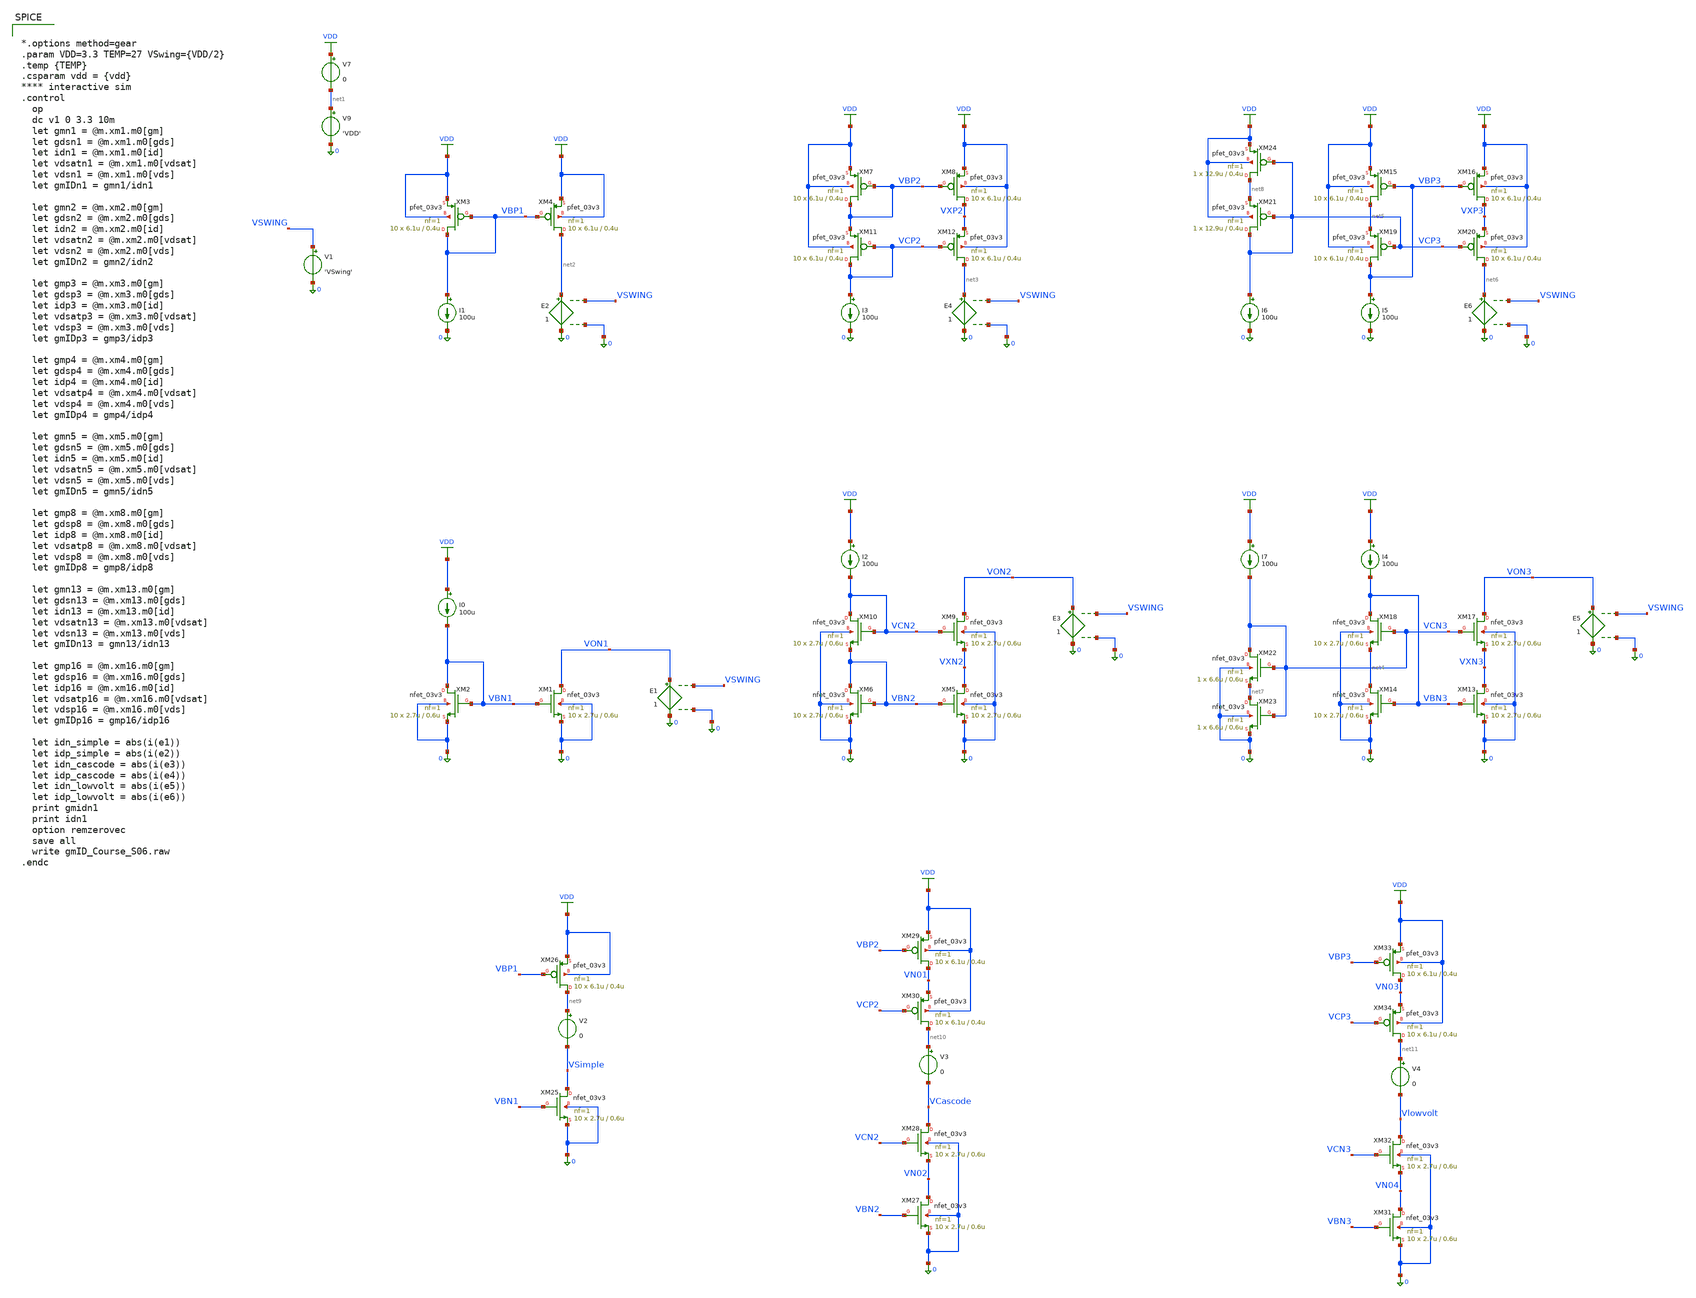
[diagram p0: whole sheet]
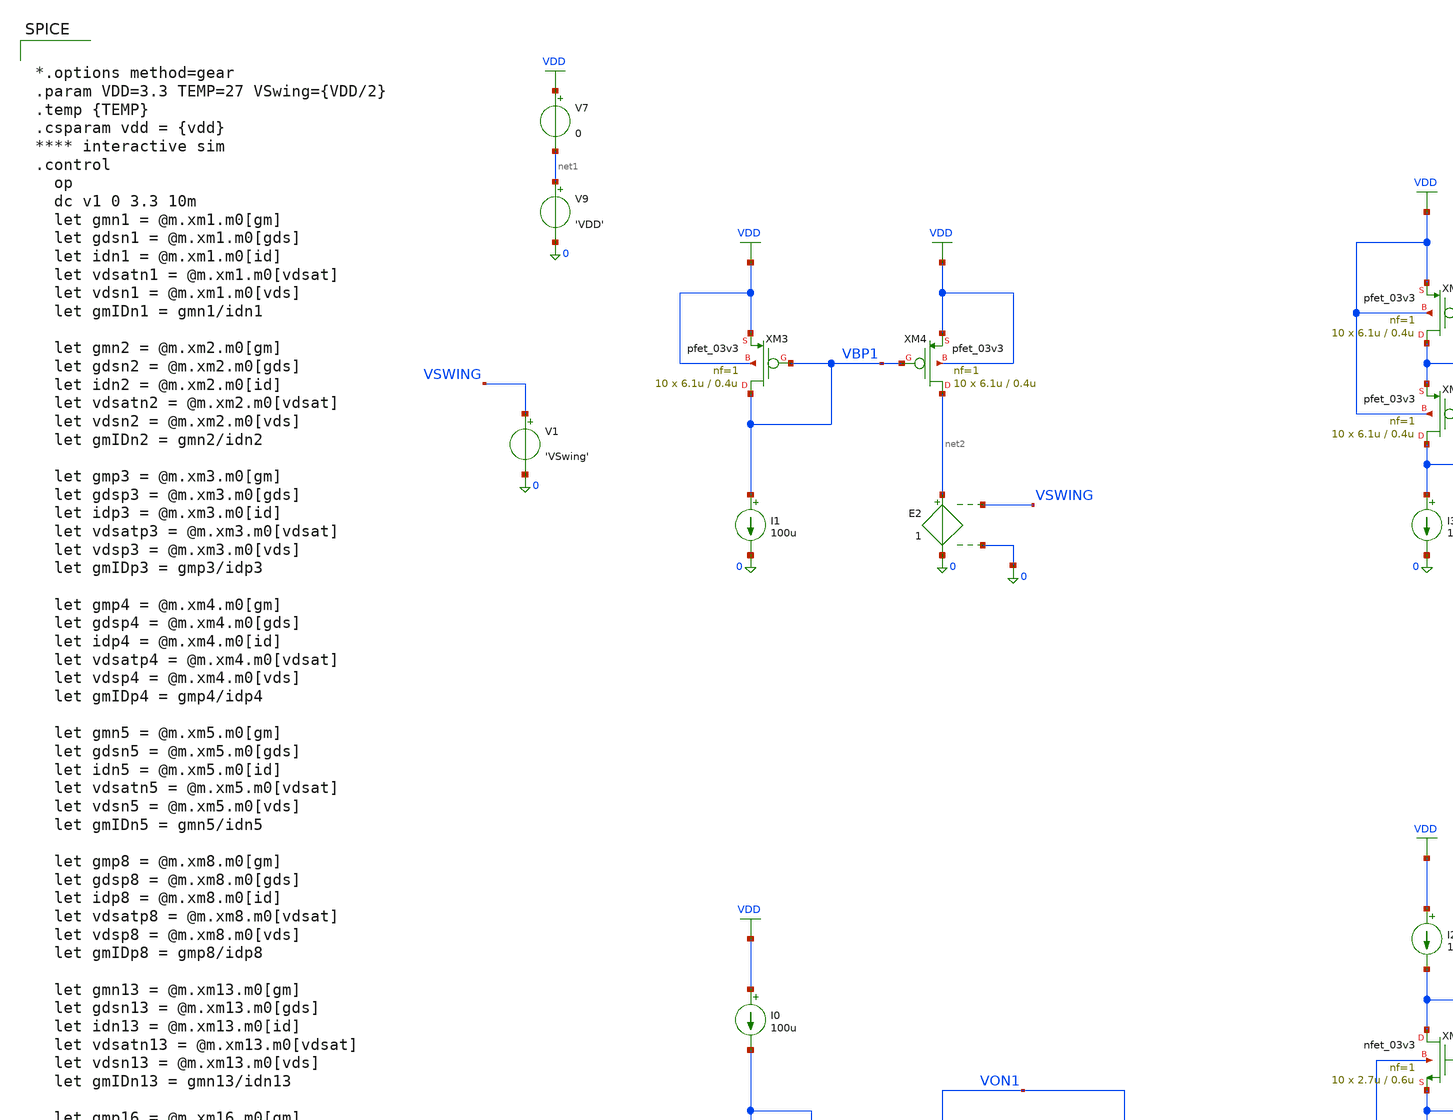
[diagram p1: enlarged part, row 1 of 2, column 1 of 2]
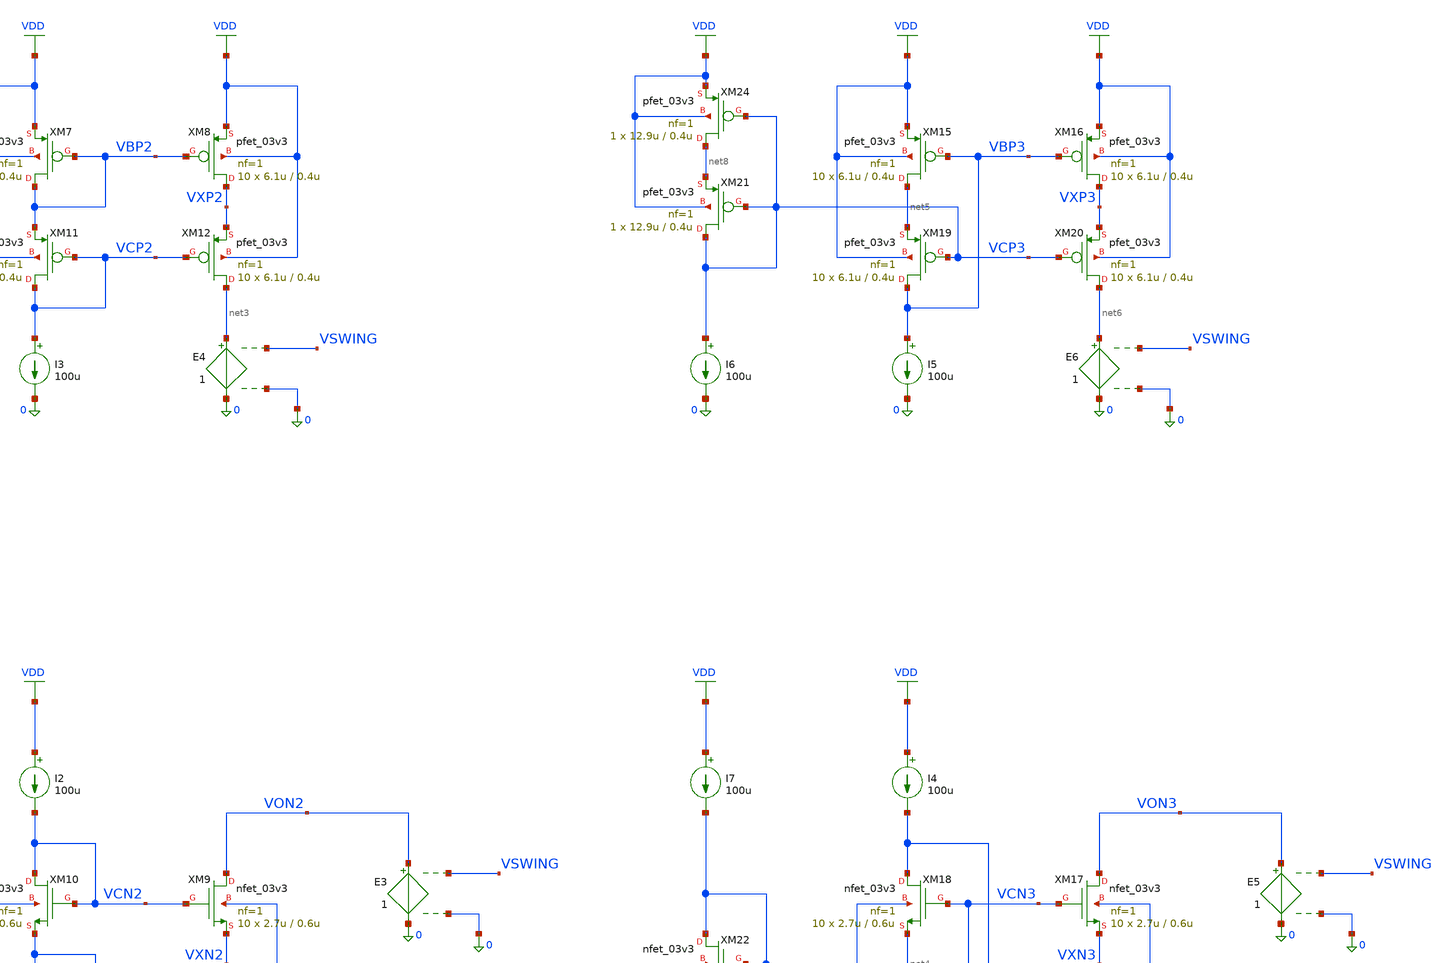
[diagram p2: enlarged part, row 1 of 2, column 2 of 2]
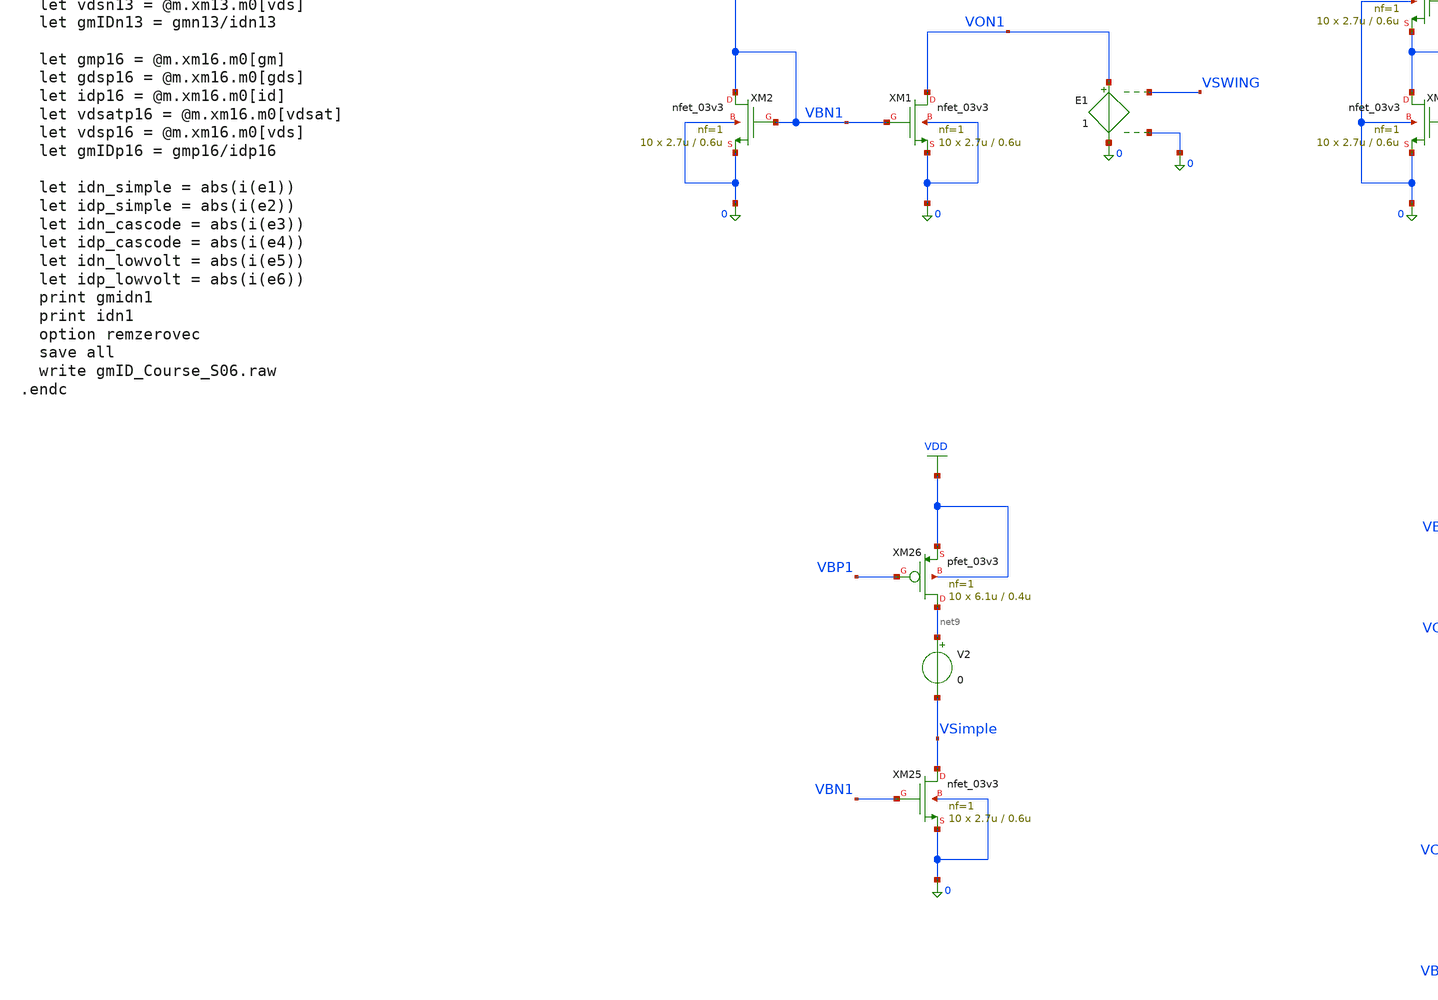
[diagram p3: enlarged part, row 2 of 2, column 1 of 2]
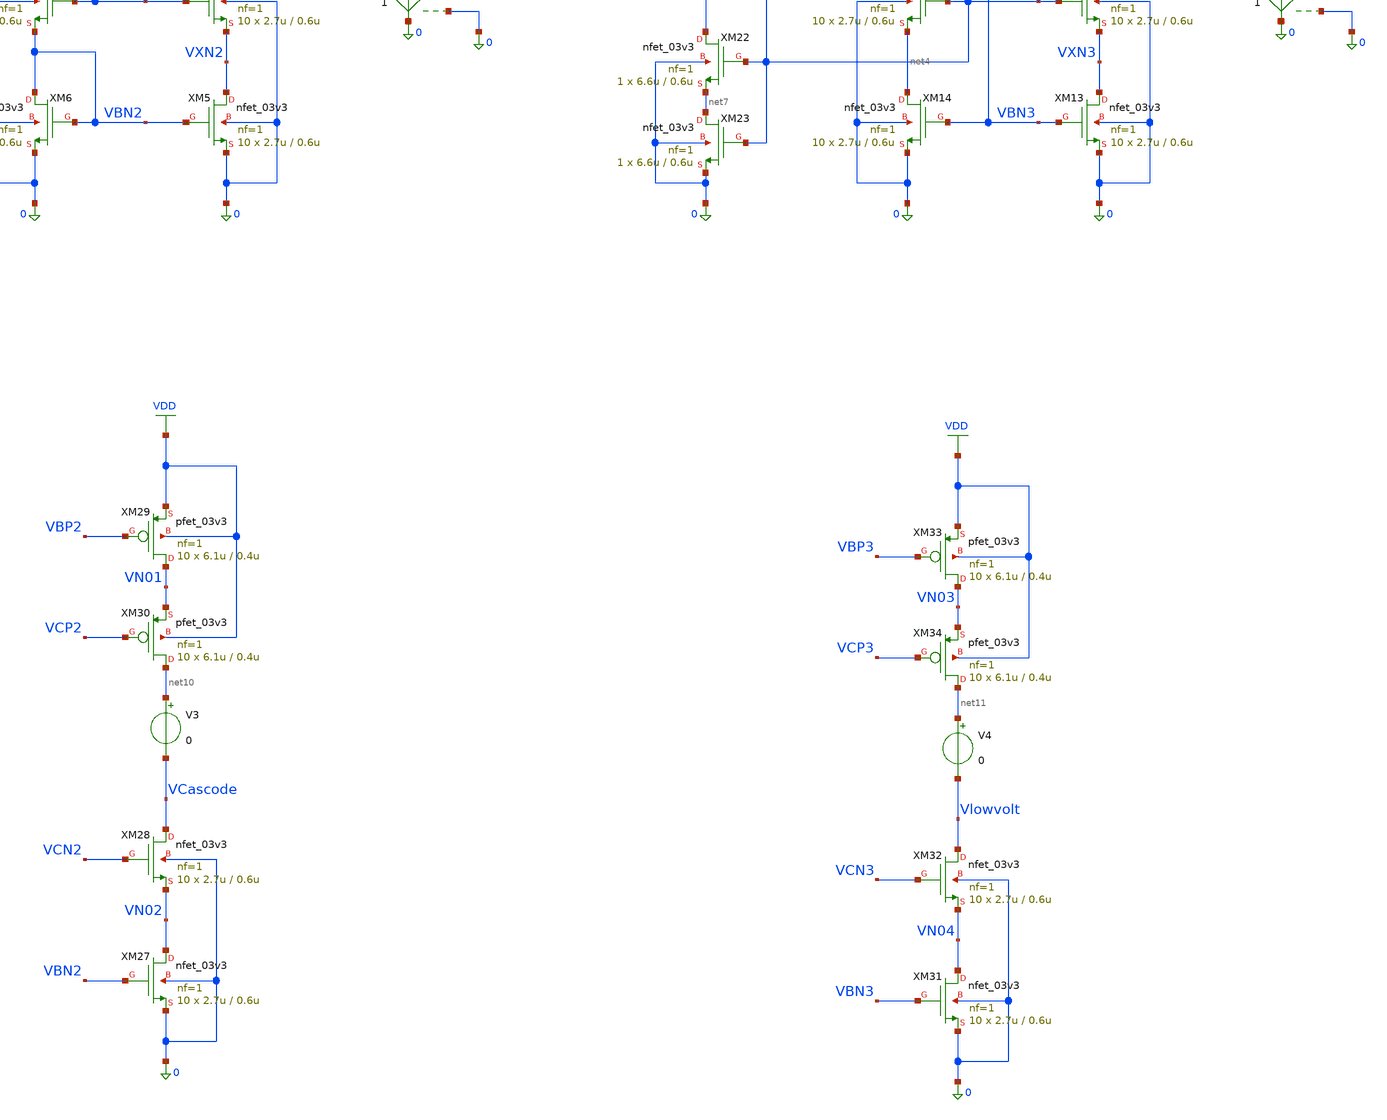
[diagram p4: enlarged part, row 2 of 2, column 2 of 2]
** sch_path: Xschem/gf180mcuD/gmID_Designs/gmID_Course_S06.sch
**.subckt gmID_Course_S06
XM1 VON1 VBN1 0 0 nfet_03v3 L=0.6u W=2.7u nf=1 ad='int((nf+1)/2) * W/nf * 0.18u' as='int((nf+2)/2) * W/nf * 0.18u'
+ pd='2*int((nf+1)/2) * (W/nf + 0.18u)' ps='2*int((nf+2)/2) * (W/nf + 0.18u)' nrd='0.18u / W' nrs='0.18u / W'
+ sa=0 sb=0 sd=0 m=10
V9 net1 0 'VDD'
V7 VDD net1 0
XM2 VBN1 VBN1 0 0 nfet_03v3 L=0.6u W=2.7u nf=1 ad='int((nf+1)/2) * W/nf * 0.18u' as='int((nf+2)/2) * W/nf * 0.18u'
+ pd='2*int((nf+1)/2) * (W/nf + 0.18u)' ps='2*int((nf+2)/2) * (W/nf + 0.18u)' nrd='0.18u / W' nrs='0.18u / W'
+ sa=0 sb=0 sd=0 m=10
I0 VDD VBN1 100u
V1 VSWING 0 'VSwing'
I1 VBP1 0 100u
XM3 VBP1 VBP1 VDD VDD pfet_03v3 L=0.4u W=6.1u nf=1 ad='int((nf+1)/2) * W/nf * 0.18u' as='int((nf+2)/2) * W/nf * 0.18u'
+ pd='2*int((nf+1)/2) * (W/nf + 0.18u)' ps='2*int((nf+2)/2) * (W/nf + 0.18u)' nrd='0.18u / W' nrs='0.18u / W'
+ sa=0 sb=0 sd=0 m=10
XM4 net2 VBP1 VDD VDD pfet_03v3 L=0.4u W=6.1u nf=1 ad='int((nf+1)/2) * W/nf * 0.18u' as='int((nf+2)/2) * W/nf * 0.18u'
+ pd='2*int((nf+1)/2) * (W/nf + 0.18u)' ps='2*int((nf+2)/2) * (W/nf + 0.18u)' nrd='0.18u / W' nrs='0.18u / W'
+ sa=0 sb=0 sd=0 m=10
E1 VON1 0 VSWING 0 1
E2 net2 0 VSWING 0 1
XM5 VXN2 VBN2 0 0 nfet_03v3 L=0.6u W=2.7u nf=1 ad='int((nf+1)/2) * W/nf * 0.18u' as='int((nf+2)/2) * W/nf * 0.18u'
+ pd='2*int((nf+1)/2) * (W/nf + 0.18u)' ps='2*int((nf+2)/2) * (W/nf + 0.18u)' nrd='0.18u / W' nrs='0.18u / W'
+ sa=0 sb=0 sd=0 m=10
XM6 VBN2 VBN2 0 0 nfet_03v3 L=0.6u W=2.7u nf=1 ad='int((nf+1)/2) * W/nf * 0.18u' as='int((nf+2)/2) * W/nf * 0.18u'
+ pd='2*int((nf+1)/2) * (W/nf + 0.18u)' ps='2*int((nf+2)/2) * (W/nf + 0.18u)' nrd='0.18u / W' nrs='0.18u / W'
+ sa=0 sb=0 sd=0 m=10
I2 VDD VCN2 100u
I3 VCP2 0 100u
XM7 VBP2 VBP2 VDD VDD pfet_03v3 L=0.4u W=6.1u nf=1 ad='int((nf+1)/2) * W/nf * 0.18u' as='int((nf+2)/2) * W/nf * 0.18u'
+ pd='2*int((nf+1)/2) * (W/nf + 0.18u)' ps='2*int((nf+2)/2) * (W/nf + 0.18u)' nrd='0.18u / W' nrs='0.18u / W'
+ sa=0 sb=0 sd=0 m=10
XM8 VXP2 VBP2 VDD VDD pfet_03v3 L=0.4u W=6.1u nf=1 ad='int((nf+1)/2) * W/nf * 0.18u' as='int((nf+2)/2) * W/nf * 0.18u'
+ pd='2*int((nf+1)/2) * (W/nf + 0.18u)' ps='2*int((nf+2)/2) * (W/nf + 0.18u)' nrd='0.18u / W' nrs='0.18u / W'
+ sa=0 sb=0 sd=0 m=10
E3 VON2 0 VSWING 0 1
E4 net3 0 VSWING 0 1
XM9 VON2 VCN2 VXN2 0 nfet_03v3 L=0.6u W=2.7u nf=1 ad='int((nf+1)/2) * W/nf * 0.18u' as='int((nf+2)/2) * W/nf * 0.18u'
+ pd='2*int((nf+1)/2) * (W/nf + 0.18u)' ps='2*int((nf+2)/2) * (W/nf + 0.18u)' nrd='0.18u / W' nrs='0.18u / W'
+ sa=0 sb=0 sd=0 m=10
XM10 VCN2 VCN2 VBN2 0 nfet_03v3 L=0.6u W=2.7u nf=1 ad='int((nf+1)/2) * W/nf * 0.18u' as='int((nf+2)/2) * W/nf * 0.18u'
+ pd='2*int((nf+1)/2) * (W/nf + 0.18u)' ps='2*int((nf+2)/2) * (W/nf + 0.18u)' nrd='0.18u / W' nrs='0.18u / W'
+ sa=0 sb=0 sd=0 m=10
XM11 VCP2 VCP2 VBP2 VDD pfet_03v3 L=0.4u W=6.1u nf=1 ad='int((nf+1)/2) * W/nf * 0.18u' as='int((nf+2)/2) * W/nf * 0.18u'
+ pd='2*int((nf+1)/2) * (W/nf + 0.18u)' ps='2*int((nf+2)/2) * (W/nf + 0.18u)' nrd='0.18u / W' nrs='0.18u / W'
+ sa=0 sb=0 sd=0 m=10
XM12 net3 VCP2 VXP2 VDD pfet_03v3 L=0.4u W=6.1u nf=1 ad='int((nf+1)/2) * W/nf * 0.18u' as='int((nf+2)/2) * W/nf * 0.18u'
+ pd='2*int((nf+1)/2) * (W/nf + 0.18u)' ps='2*int((nf+2)/2) * (W/nf + 0.18u)' nrd='0.18u / W' nrs='0.18u / W'
+ sa=0 sb=0 sd=0 m=10
XM13 VXN3 VBN3 0 0 nfet_03v3 L=0.6u W=2.7u nf=1 ad='int((nf+1)/2) * W/nf * 0.18u' as='int((nf+2)/2) * W/nf * 0.18u'
+ pd='2*int((nf+1)/2) * (W/nf + 0.18u)' ps='2*int((nf+2)/2) * (W/nf + 0.18u)' nrd='0.18u / W' nrs='0.18u / W'
+ sa=0 sb=0 sd=0 m=10
XM14 net4 VBN3 0 0 nfet_03v3 L=0.6u W=2.7u nf=1 ad='int((nf+1)/2) * W/nf * 0.18u' as='int((nf+2)/2) * W/nf * 0.18u'
+ pd='2*int((nf+1)/2) * (W/nf + 0.18u)' ps='2*int((nf+2)/2) * (W/nf + 0.18u)' nrd='0.18u / W' nrs='0.18u / W'
+ sa=0 sb=0 sd=0 m=10
I4 VDD VBN3 100u
I5 VBP3 0 100u
XM15 net5 VBP3 VDD VDD pfet_03v3 L=0.4u W=6.1u nf=1 ad='int((nf+1)/2) * W/nf * 0.18u' as='int((nf+2)/2) * W/nf * 0.18u'
+ pd='2*int((nf+1)/2) * (W/nf + 0.18u)' ps='2*int((nf+2)/2) * (W/nf + 0.18u)' nrd='0.18u / W' nrs='0.18u / W'
+ sa=0 sb=0 sd=0 m=10
XM16 VXP3 VBP3 VDD VDD pfet_03v3 L=0.4u W=6.1u nf=1 ad='int((nf+1)/2) * W/nf * 0.18u' as='int((nf+2)/2) * W/nf * 0.18u'
+ pd='2*int((nf+1)/2) * (W/nf + 0.18u)' ps='2*int((nf+2)/2) * (W/nf + 0.18u)' nrd='0.18u / W' nrs='0.18u / W'
+ sa=0 sb=0 sd=0 m=10
E5 VON3 0 VSWING 0 1
E6 net6 0 VSWING 0 1
XM17 VON3 VCN3 VXN3 0 nfet_03v3 L=0.6u W=2.7u nf=1 ad='int((nf+1)/2) * W/nf * 0.18u' as='int((nf+2)/2) * W/nf * 0.18u'
+ pd='2*int((nf+1)/2) * (W/nf + 0.18u)' ps='2*int((nf+2)/2) * (W/nf + 0.18u)' nrd='0.18u / W' nrs='0.18u / W'
+ sa=0 sb=0 sd=0 m=10
XM18 VBN3 VCN3 net4 0 nfet_03v3 L=0.6u W=2.7u nf=1 ad='int((nf+1)/2) * W/nf * 0.18u' as='int((nf+2)/2) * W/nf * 0.18u'
+ pd='2*int((nf+1)/2) * (W/nf + 0.18u)' ps='2*int((nf+2)/2) * (W/nf + 0.18u)' nrd='0.18u / W' nrs='0.18u / W'
+ sa=0 sb=0 sd=0 m=10
XM19 VBP3 VCP3 net5 VDD pfet_03v3 L=0.4u W=6.1u nf=1 ad='int((nf+1)/2) * W/nf * 0.18u' as='int((nf+2)/2) * W/nf * 0.18u'
+ pd='2*int((nf+1)/2) * (W/nf + 0.18u)' ps='2*int((nf+2)/2) * (W/nf + 0.18u)' nrd='0.18u / W' nrs='0.18u / W'
+ sa=0 sb=0 sd=0 m=10
XM20 net6 VCP3 VXP3 VDD pfet_03v3 L=0.4u W=6.1u nf=1 ad='int((nf+1)/2) * W/nf * 0.18u' as='int((nf+2)/2) * W/nf * 0.18u'
+ pd='2*int((nf+1)/2) * (W/nf + 0.18u)' ps='2*int((nf+2)/2) * (W/nf + 0.18u)' nrd='0.18u / W' nrs='0.18u / W'
+ sa=0 sb=0 sd=0 m=10
I6 VCP3 0 100u
XM21 VCP3 VCP3 net8 VDD pfet_03v3 L=0.4u W=12.9u nf=1 ad='int((nf+1)/2) * W/nf * 0.18u' as='int((nf+2)/2) * W/nf * 0.18u'
+ pd='2*int((nf+1)/2) * (W/nf + 0.18u)' ps='2*int((nf+2)/2) * (W/nf + 0.18u)' nrd='0.18u / W' nrs='0.18u / W'
+ sa=0 sb=0 sd=0 m=1
XM22 VCN3 VCN3 net7 0 nfet_03v3 L=0.6u W=6.6u nf=1 ad='int((nf+1)/2) * W/nf * 0.18u' as='int((nf+2)/2) * W/nf * 0.18u'
+ pd='2*int((nf+1)/2) * (W/nf + 0.18u)' ps='2*int((nf+2)/2) * (W/nf + 0.18u)' nrd='0.18u / W' nrs='0.18u / W'
+ sa=0 sb=0 sd=0 m=1
I7 VDD VCN3 100u
XM23 net7 VCN3 0 0 nfet_03v3 L=0.6u W=6.6u nf=1 ad='int((nf+1)/2) * W/nf * 0.18u' as='int((nf+2)/2) * W/nf * 0.18u'
+ pd='2*int((nf+1)/2) * (W/nf + 0.18u)' ps='2*int((nf+2)/2) * (W/nf + 0.18u)' nrd='0.18u / W' nrs='0.18u / W'
+ sa=0 sb=0 sd=0 m=1
XM24 net8 VCP3 VDD VDD pfet_03v3 L=0.4u W=12.9u nf=1 ad='int((nf+1)/2) * W/nf * 0.18u' as='int((nf+2)/2) * W/nf * 0.18u'
+ pd='2*int((nf+1)/2) * (W/nf + 0.18u)' ps='2*int((nf+2)/2) * (W/nf + 0.18u)' nrd='0.18u / W' nrs='0.18u / W'
+ sa=0 sb=0 sd=0 m=1
XM25 VSimple VBN1 0 0 nfet_03v3 L=0.6u W=2.7u nf=1 ad='int((nf+1)/2) * W/nf * 0.18u' as='int((nf+2)/2) * W/nf * 0.18u'
+ pd='2*int((nf+1)/2) * (W/nf + 0.18u)' ps='2*int((nf+2)/2) * (W/nf + 0.18u)' nrd='0.18u / W' nrs='0.18u / W'
+ sa=0 sb=0 sd=0 m=10
XM26 net9 VBP1 VDD VDD pfet_03v3 L=0.4u W=6.1u nf=1 ad='int((nf+1)/2) * W/nf * 0.18u' as='int((nf+2)/2) * W/nf * 0.18u'
+ pd='2*int((nf+1)/2) * (W/nf + 0.18u)' ps='2*int((nf+2)/2) * (W/nf + 0.18u)' nrd='0.18u / W' nrs='0.18u / W'
+ sa=0 sb=0 sd=0 m=10
V2 net9 VSimple 0
XM27 VN02 VBN2 0 0 nfet_03v3 L=0.6u W=2.7u nf=1 ad='int((nf+1)/2) * W/nf * 0.18u' as='int((nf+2)/2) * W/nf * 0.18u'
+ pd='2*int((nf+1)/2) * (W/nf + 0.18u)' ps='2*int((nf+2)/2) * (W/nf + 0.18u)' nrd='0.18u / W' nrs='0.18u / W'
+ sa=0 sb=0 sd=0 m=10
XM28 VCascode VCN2 VN02 0 nfet_03v3 L=0.6u W=2.7u nf=1 ad='int((nf+1)/2) * W/nf * 0.18u' as='int((nf+2)/2) * W/nf * 0.18u'
+ pd='2*int((nf+1)/2) * (W/nf + 0.18u)' ps='2*int((nf+2)/2) * (W/nf + 0.18u)' nrd='0.18u / W' nrs='0.18u / W'
+ sa=0 sb=0 sd=0 m=10
XM29 VN01 VBP2 VDD VDD pfet_03v3 L=0.4u W=6.1u nf=1 ad='int((nf+1)/2) * W/nf * 0.18u' as='int((nf+2)/2) * W/nf * 0.18u'
+ pd='2*int((nf+1)/2) * (W/nf + 0.18u)' ps='2*int((nf+2)/2) * (W/nf + 0.18u)' nrd='0.18u / W' nrs='0.18u / W'
+ sa=0 sb=0 sd=0 m=10
XM30 net10 VCP2 VN01 VDD pfet_03v3 L=0.4u W=6.1u nf=1 ad='int((nf+1)/2) * W/nf * 0.18u' as='int((nf+2)/2) * W/nf * 0.18u'
+ pd='2*int((nf+1)/2) * (W/nf + 0.18u)' ps='2*int((nf+2)/2) * (W/nf + 0.18u)' nrd='0.18u / W' nrs='0.18u / W'
+ sa=0 sb=0 sd=0 m=10
V3 net10 VCascode 0
XM31 VN04 VBN3 0 0 nfet_03v3 L=0.6u W=2.7u nf=1 ad='int((nf+1)/2) * W/nf * 0.18u' as='int((nf+2)/2) * W/nf * 0.18u'
+ pd='2*int((nf+1)/2) * (W/nf + 0.18u)' ps='2*int((nf+2)/2) * (W/nf + 0.18u)' nrd='0.18u / W' nrs='0.18u / W'
+ sa=0 sb=0 sd=0 m=10
XM32 Vlowvolt VCN3 VN04 0 nfet_03v3 L=0.6u W=2.7u nf=1 ad='int((nf+1)/2) * W/nf * 0.18u' as='int((nf+2)/2) * W/nf * 0.18u'
+ pd='2*int((nf+1)/2) * (W/nf + 0.18u)' ps='2*int((nf+2)/2) * (W/nf + 0.18u)' nrd='0.18u / W' nrs='0.18u / W'
+ sa=0 sb=0 sd=0 m=10
XM33 VN03 VBP3 VDD VDD pfet_03v3 L=0.4u W=6.1u nf=1 ad='int((nf+1)/2) * W/nf * 0.18u' as='int((nf+2)/2) * W/nf * 0.18u'
+ pd='2*int((nf+1)/2) * (W/nf + 0.18u)' ps='2*int((nf+2)/2) * (W/nf + 0.18u)' nrd='0.18u / W' nrs='0.18u / W'
+ sa=0 sb=0 sd=0 m=10
XM34 net11 VCP3 VN03 VDD pfet_03v3 L=0.4u W=6.1u nf=1 ad='int((nf+1)/2) * W/nf * 0.18u' as='int((nf+2)/2) * W/nf * 0.18u'
+ pd='2*int((nf+1)/2) * (W/nf + 0.18u)' ps='2*int((nf+2)/2) * (W/nf + 0.18u)' nrd='0.18u / W' nrs='0.18u / W'
+ sa=0 sb=0 sd=0 m=10
V4 net11 Vlowvolt 0
**** begin user architecture code

.include $::180MCU_MODELS/design.ngspice
.lib $::180MCU_MODELS/sm141064.ngspice typical
.param sw_stat_global=0
.param sw_stat_mismatch=0



*.options method=gear
.param VDD=3.3 TEMP=27 VSwing={VDD/2}
.temp {TEMP}
.csparam vdd = {vdd}
**** interactive sim
.control
  op
  dc v1 0 3.3 10m
  let gmn1 = @m.xm1.m0[gm]
  let gdsn1 = @m.xm1.m0[gds]
  let idn1 = @m.xm1.m0[id]
  let vdsatn1 = @m.xm1.m0[vdsat]
  let vdsn1 = @m.xm1.m0[vds]
  let gmIDn1 = gmn1/idn1

  let gmn2 = @m.xm2.m0[gm]
  let gdsn2 = @m.xm2.m0[gds]
  let idn2 = @m.xm2.m0[id]
  let vdsatn2 = @m.xm2.m0[vdsat]
  let vdsn2 = @m.xm2.m0[vds]
  let gmIDn2 = gmn2/idn2

  let gmp3 = @m.xm3.m0[gm]
  let gdsp3 = @m.xm3.m0[gds]
  let idp3 = @m.xm3.m0[id]
  let vdsatp3 = @m.xm3.m0[vdsat]
  let vdsp3 = @m.xm3.m0[vds]
  let gmIDp3 = gmp3/idp3

  let gmp4 = @m.xm4.m0[gm]
  let gdsp4 = @m.xm4.m0[gds]
  let idp4 = @m.xm4.m0[id]
  let vdsatp4 = @m.xm4.m0[vdsat]
  let vdsp4 = @m.xm4.m0[vds]
  let gmIDp4 = gmp4/idp4

  let gmn5 = @m.xm5.m0[gm]
  let gdsn5 = @m.xm5.m0[gds]
  let idn5 = @m.xm5.m0[id]
  let vdsatn5 = @m.xm5.m0[vdsat]
  let vdsn5 = @m.xm5.m0[vds]
  let gmIDn5 = gmn5/idn5

  let gmp8 = @m.xm8.m0[gm]
  let gdsp8 = @m.xm8.m0[gds]
  let idp8 = @m.xm8.m0[id]
  let vdsatp8 = @m.xm8.m0[vdsat]
  let vdsp8 = @m.xm8.m0[vds]
  let gmIDp8 = gmp8/idp8

  let gmn13 = @m.xm13.m0[gm]
  let gdsn13 = @m.xm13.m0[gds]
  let idn13 = @m.xm13.m0[id]
  let vdsatn13 = @m.xm13.m0[vdsat]
  let vdsn13 = @m.xm13.m0[vds]
  let gmIDn13 = gmn13/idn13

  let gmp16 = @m.xm16.m0[gm]
  let gdsp16 = @m.xm16.m0[gds]
  let idp16 = @m.xm16.m0[id]
  let vdsatp16 = @m.xm16.m0[vdsat]
  let vdsp16 = @m.xm16.m0[vds]
  let gmIDp16 = gmp16/idp16

  let idn_simple = abs(i(e1))
  let idp_simple = abs(i(e2))
  let idn_cascode = abs(i(e3))
  let idp_cascode = abs(i(e4))
  let idn_lowvolt = abs(i(e5))
  let idp_lowvolt = abs(i(e6))
  print gmidn1
  print idn1
  option remzerovec
  save all
  write gmID_Course_S06.raw
.endc


**** end user architecture code
**.ends
.GLOBAL VDD
.end
